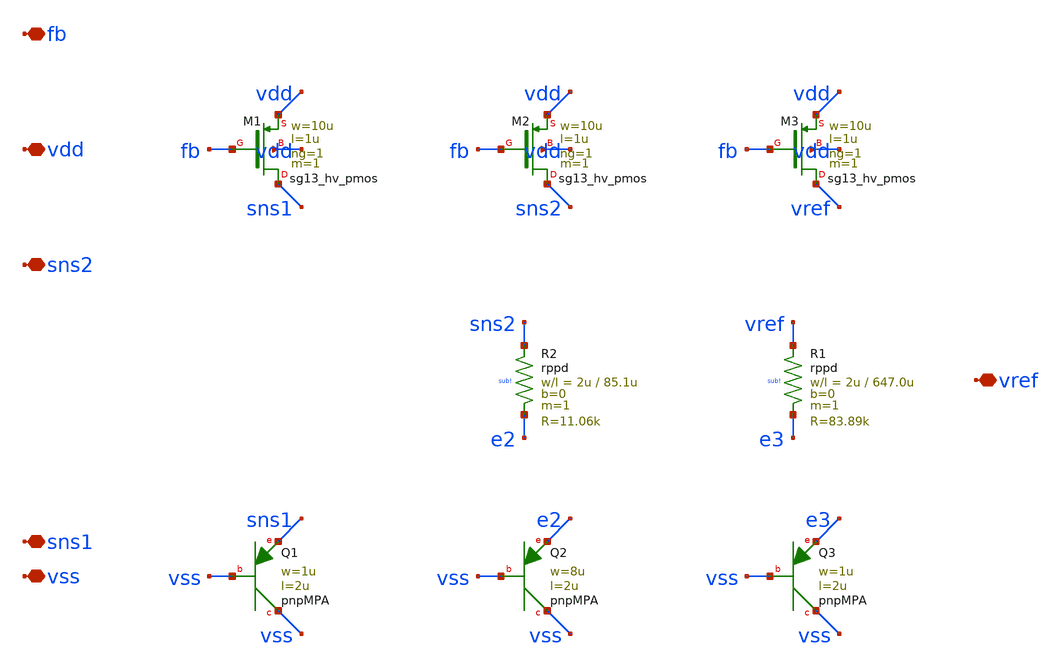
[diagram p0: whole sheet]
** sch_path: design/sg13cmos5l/bandgap_core.sch
**.subckt bandgap_core vdd vss fb sns1 sns2 vref
*.iopin vdd
*.iopin vss
*.iopin fb
*.iopin sns1
*.iopin sns2
*.iopin vref
XM1 sns1 fb vdd vdd sg13_hv_pmos w=10u l=1u ng=1 m=1 mm_ok=1
XQ1 vss vss sns1 pnpMPA a=2p p=6u m=1
XM2 sns2 fb vdd vdd sg13_hv_pmos w=10u l=1u ng=1 m=1 mm_ok=1
XR2 sns2 e2 sub! rppd w=2u l=85.1u m=1 b=0 mm_ok=1
XQ2 vss vss e2 pnpMPA a=16p p=20u m=1
XM3 vref fb vdd vdd sg13_hv_pmos w=10u l=1u ng=1 m=1 mm_ok=1
XR1 vref e3 sub! rppd w=2u l=647.0u m=1 b=0 mm_ok=1
XQ3 vss vss e3 pnpMPA a=2p p=6u m=1
**.ends
.end
